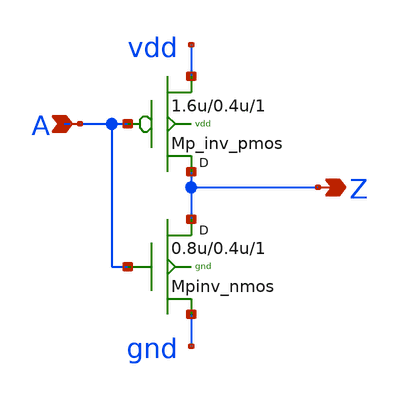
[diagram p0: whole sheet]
** sch_path: sram_4_16_scn4m/pinv_5.sch
**.subckt pinv_5 A Z
*.ipin A
*.opin Z
Mpinv_nmos Z A gnd gnd n w=0.8u l=0.4u m=1
Mp_inv_pmos Z A vdd vdd p w=1.6u l=0.4u m=1
**.ends
.end
